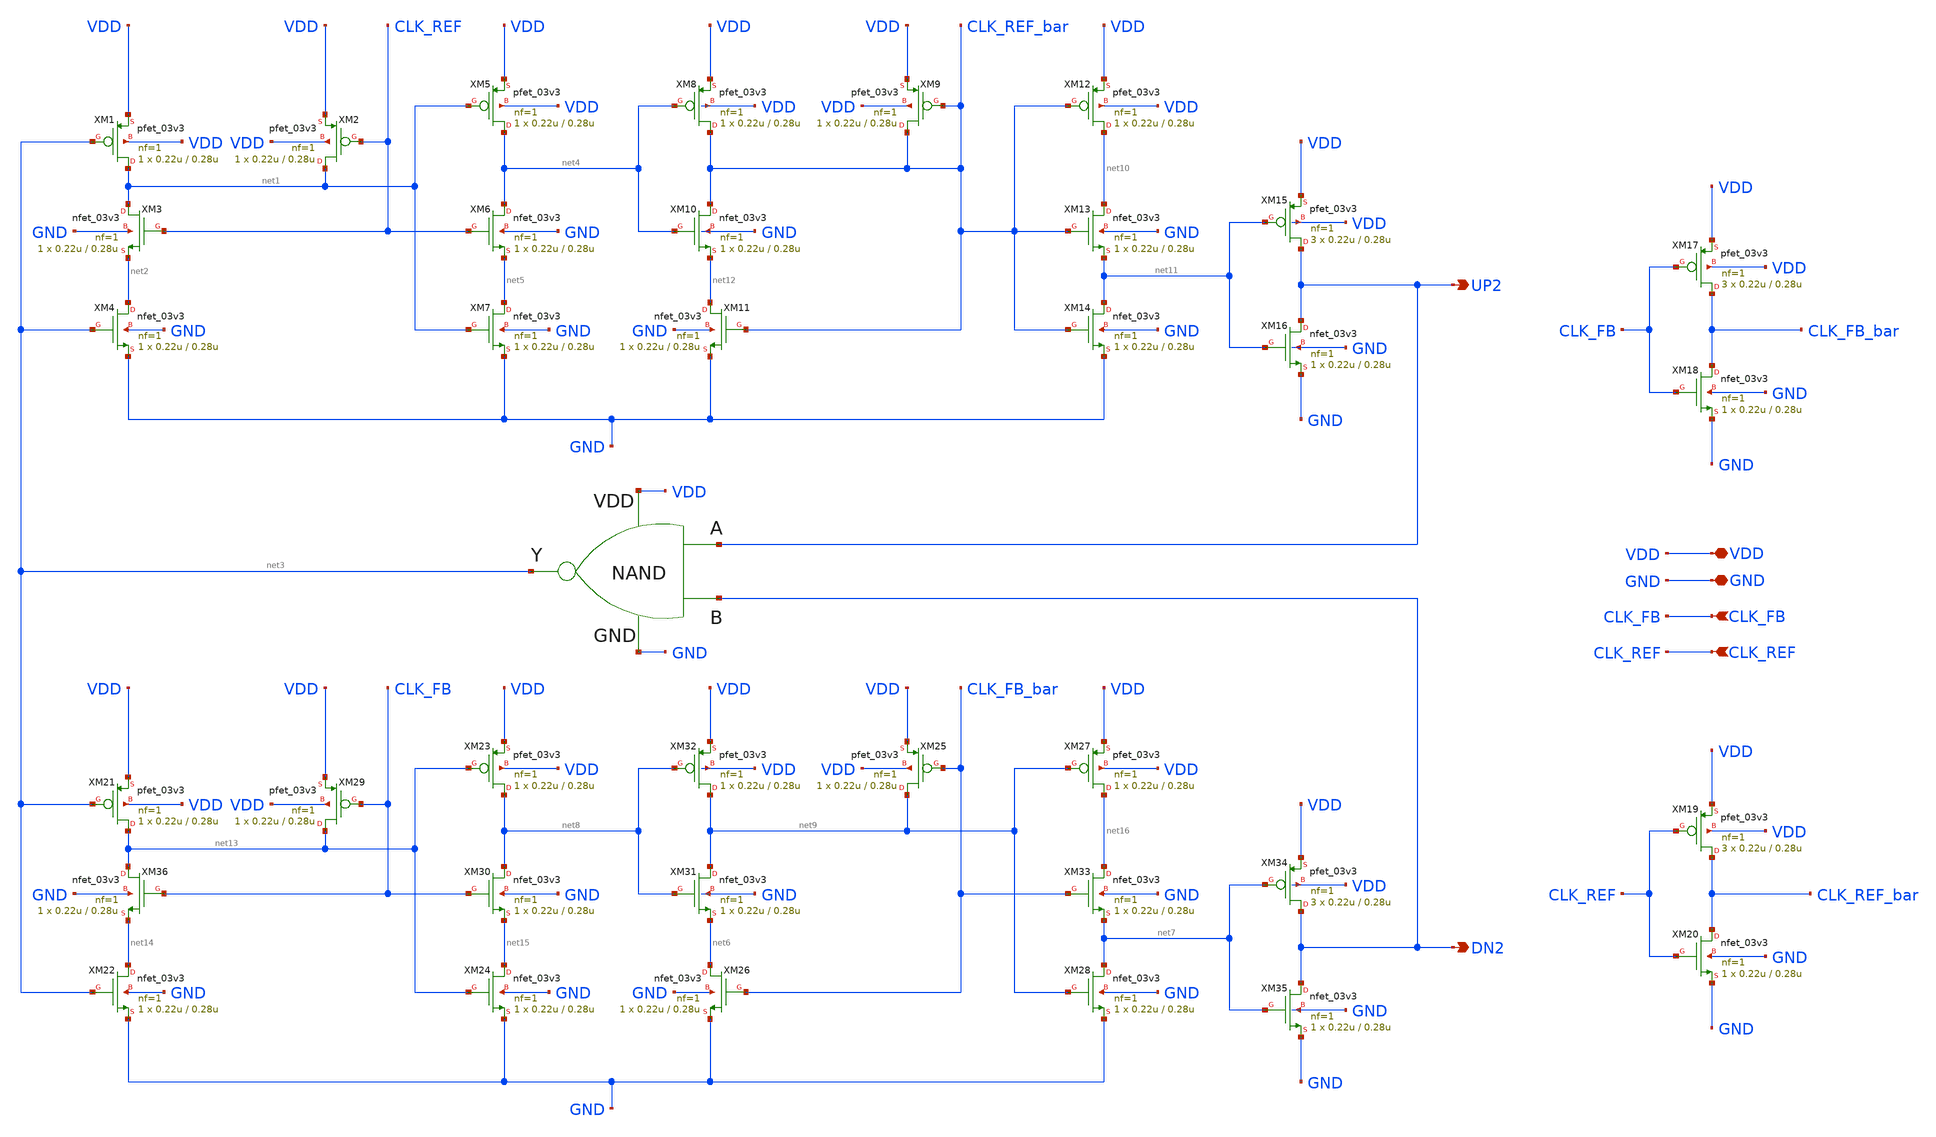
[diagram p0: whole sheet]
** sch_path: PFD/OPL_PFD.sch
**.subckt OPL_PFD UP2 CLK_FB CLK_REF DN2 VDD GND
*.opin UP2
*.ipin CLK_FB
*.ipin CLK_REF
*.opin DN2
*.iopin VDD
*.iopin GND
XM1 net1 net3 VDD VDD pfet_03v3 L=0.28u W=0.22u nf=1 ad='int((nf+1)/2) * W/nf * 0.18u' as='int((nf+2)/2) * W/nf * 0.18u'
+ pd='2*int((nf+1)/2) * (W/nf + 0.18u)' ps='2*int((nf+2)/2) * (W/nf + 0.18u)' nrd='0.18u / W' nrs='0.18u / W'
+ sa=0 sb=0 sd=0 m=1
XM4 net2 net3 GND GND nfet_03v3 L=0.28u W=0.22u nf=1 ad='int((nf+1)/2) * W/nf * 0.18u' as='int((nf+2)/2) * W/nf * 0.18u'
+ pd='2*int((nf+1)/2) * (W/nf + 0.18u)' ps='2*int((nf+2)/2) * (W/nf + 0.18u)' nrd='0.18u / W' nrs='0.18u / W'
+ sa=0 sb=0 sd=0 m=1
XM5 net4 net1 VDD VDD pfet_03v3 L=0.28u W=0.22u nf=1 ad='int((nf+1)/2) * W/nf * 0.18u' as='int((nf+2)/2) * W/nf * 0.18u'
+ pd='2*int((nf+1)/2) * (W/nf + 0.18u)' ps='2*int((nf+2)/2) * (W/nf + 0.18u)' nrd='0.18u / W' nrs='0.18u / W'
+ sa=0 sb=0 sd=0 m=1
XM7 net5 net1 GND GND nfet_03v3 L=0.28u W=0.22u nf=1 ad='int((nf+1)/2) * W/nf * 0.18u' as='int((nf+2)/2) * W/nf * 0.18u'
+ pd='2*int((nf+1)/2) * (W/nf + 0.18u)' ps='2*int((nf+2)/2) * (W/nf + 0.18u)' nrd='0.18u / W' nrs='0.18u / W'
+ sa=0 sb=0 sd=0 m=1
XM9 CLK_REF_bar CLK_REF_bar VDD VDD pfet_03v3 L=0.28u W=0.22u nf=1 ad='int((nf+1)/2) * W/nf * 0.18u'
+ as='int((nf+2)/2) * W/nf * 0.18u' pd='2*int((nf+1)/2) * (W/nf + 0.18u)' ps='2*int((nf+2)/2) * (W/nf + 0.18u)'
+ nrd='0.18u / W' nrs='0.18u / W' sa=0 sb=0 sd=0 m=1
XM11 net12 CLK_REF_bar GND GND nfet_03v3 L=0.28u W=0.22u nf=1 ad='int((nf+1)/2) * W/nf * 0.18u' as='int((nf+2)/2) * W/nf * 0.18u'
+ pd='2*int((nf+1)/2) * (W/nf + 0.18u)' ps='2*int((nf+2)/2) * (W/nf + 0.18u)' nrd='0.18u / W' nrs='0.18u / W'
+ sa=0 sb=0 sd=0 m=1
XM12 net10 CLK_REF_bar VDD VDD pfet_03v3 L=0.28u W=0.22u nf=1 ad='int((nf+1)/2) * W/nf * 0.18u' as='int((nf+2)/2) * W/nf * 0.18u'
+ pd='2*int((nf+1)/2) * (W/nf + 0.18u)' ps='2*int((nf+2)/2) * (W/nf + 0.18u)' nrd='0.18u / W' nrs='0.18u / W'
+ sa=0 sb=0 sd=0 m=1
XM14 net11 CLK_REF_bar GND GND nfet_03v3 L=0.28u W=0.22u nf=1 ad='int((nf+1)/2) * W/nf * 0.18u' as='int((nf+2)/2) * W/nf * 0.18u'
+ pd='2*int((nf+1)/2) * (W/nf + 0.18u)' ps='2*int((nf+2)/2) * (W/nf + 0.18u)' nrd='0.18u / W' nrs='0.18u / W'
+ sa=0 sb=0 sd=0 m=1
XM2 net1 CLK_REF VDD VDD pfet_03v3 L=0.28u W=0.22u nf=1 ad='int((nf+1)/2) * W/nf * 0.18u' as='int((nf+2)/2) * W/nf * 0.18u'
+ pd='2*int((nf+1)/2) * (W/nf + 0.18u)' ps='2*int((nf+2)/2) * (W/nf + 0.18u)' nrd='0.18u / W' nrs='0.18u / W'
+ sa=0 sb=0 sd=0 m=1
XM6 net4 CLK_REF net5 GND nfet_03v3 L=0.28u W=0.22u nf=1 ad='int((nf+1)/2) * W/nf * 0.18u' as='int((nf+2)/2) * W/nf * 0.18u'
+ pd='2*int((nf+1)/2) * (W/nf + 0.18u)' ps='2*int((nf+2)/2) * (W/nf + 0.18u)' nrd='0.18u / W' nrs='0.18u / W'
+ sa=0 sb=0 sd=0 m=1
XM10 CLK_REF_bar net4 net12 GND nfet_03v3 L=0.28u W=0.22u nf=1 ad='int((nf+1)/2) * W/nf * 0.18u' as='int((nf+2)/2) * W/nf * 0.18u'
+ pd='2*int((nf+1)/2) * (W/nf + 0.18u)' ps='2*int((nf+2)/2) * (W/nf + 0.18u)' nrd='0.18u / W' nrs='0.18u / W'
+ sa=0 sb=0 sd=0 m=1
XM8 CLK_REF_bar net4 VDD VDD pfet_03v3 L=0.28u W=0.22u nf=1 ad='int((nf+1)/2) * W/nf * 0.18u' as='int((nf+2)/2) * W/nf * 0.18u'
+ pd='2*int((nf+1)/2) * (W/nf + 0.18u)' ps='2*int((nf+2)/2) * (W/nf + 0.18u)' nrd='0.18u / W' nrs='0.18u / W'
+ sa=0 sb=0 sd=0 m=1
XM13 net10 CLK_REF_bar net11 GND nfet_03v3 L=0.28u W=0.22u nf=1 ad='int((nf+1)/2) * W/nf * 0.18u' as='int((nf+2)/2) * W/nf * 0.18u'
+ pd='2*int((nf+1)/2) * (W/nf + 0.18u)' ps='2*int((nf+2)/2) * (W/nf + 0.18u)' nrd='0.18u / W' nrs='0.18u / W'
+ sa=0 sb=0 sd=0 m=1
XM15 UP2 net11 VDD VDD pfet_03v3 L=0.28u W=0.22u nf=1 ad='int((nf+1)/2) * W/nf * 0.18u' as='int((nf+2)/2) * W/nf * 0.18u'
+ pd='2*int((nf+1)/2) * (W/nf + 0.18u)' ps='2*int((nf+2)/2) * (W/nf + 0.18u)' nrd='0.18u / W' nrs='0.18u / W'
+ sa=0 sb=0 sd=0 m=3
XM16 UP2 net11 GND GND nfet_03v3 L=0.28u W=0.22u nf=1 ad='int((nf+1)/2) * W/nf * 0.18u' as='int((nf+2)/2) * W/nf * 0.18u'
+ pd='2*int((nf+1)/2) * (W/nf + 0.18u)' ps='2*int((nf+2)/2) * (W/nf + 0.18u)' nrd='0.18u / W' nrs='0.18u / W'
+ sa=0 sb=0 sd=0 m=1
XM17 CLK_FB_bar CLK_FB VDD VDD pfet_03v3 L=0.28u W=0.22u nf=1 ad='int((nf+1)/2) * W/nf * 0.18u' as='int((nf+2)/2) * W/nf * 0.18u'
+ pd='2*int((nf+1)/2) * (W/nf + 0.18u)' ps='2*int((nf+2)/2) * (W/nf + 0.18u)' nrd='0.18u / W' nrs='0.18u / W'
+ sa=0 sb=0 sd=0 m=3
XM18 CLK_FB_bar CLK_FB GND GND nfet_03v3 L=0.28u W=0.22u nf=1 ad='int((nf+1)/2) * W/nf * 0.18u' as='int((nf+2)/2) * W/nf * 0.18u'
+ pd='2*int((nf+1)/2) * (W/nf + 0.18u)' ps='2*int((nf+2)/2) * (W/nf + 0.18u)' nrd='0.18u / W' nrs='0.18u / W'
+ sa=0 sb=0 sd=0 m=1
XM19 CLK_REF_bar CLK_REF VDD VDD pfet_03v3 L=0.28u W=0.22u nf=1 ad='int((nf+1)/2) * W/nf * 0.18u' as='int((nf+2)/2) * W/nf * 0.18u'
+ pd='2*int((nf+1)/2) * (W/nf + 0.18u)' ps='2*int((nf+2)/2) * (W/nf + 0.18u)' nrd='0.18u / W' nrs='0.18u / W'
+ sa=0 sb=0 sd=0 m=3
XM20 CLK_REF_bar CLK_REF GND GND nfet_03v3 L=0.28u W=0.22u nf=1 ad='int((nf+1)/2) * W/nf * 0.18u' as='int((nf+2)/2) * W/nf * 0.18u'
+ pd='2*int((nf+1)/2) * (W/nf + 0.18u)' ps='2*int((nf+2)/2) * (W/nf + 0.18u)' nrd='0.18u / W' nrs='0.18u / W'
+ sa=0 sb=0 sd=0 m=1
XM3 net1 CLK_REF net2 GND nfet_03v3 L=0.28u W=0.22u nf=1 ad='int((nf+1)/2) * W/nf * 0.18u' as='int((nf+2)/2) * W/nf * 0.18u'
+ pd='2*int((nf+1)/2) * (W/nf + 0.18u)' ps='2*int((nf+2)/2) * (W/nf + 0.18u)' nrd='0.18u / W' nrs='0.18u / W'
+ sa=0 sb=0 sd=0 m=1
XM21 net13 net3 VDD VDD pfet_03v3 L=0.28u W=0.22u nf=1 ad='int((nf+1)/2) * W/nf * 0.18u' as='int((nf+2)/2) * W/nf * 0.18u'
+ pd='2*int((nf+1)/2) * (W/nf + 0.18u)' ps='2*int((nf+2)/2) * (W/nf + 0.18u)' nrd='0.18u / W' nrs='0.18u / W'
+ sa=0 sb=0 sd=0 m=1
XM22 net14 net3 GND GND nfet_03v3 L=0.28u W=0.22u nf=1 ad='int((nf+1)/2) * W/nf * 0.18u' as='int((nf+2)/2) * W/nf * 0.18u'
+ pd='2*int((nf+1)/2) * (W/nf + 0.18u)' ps='2*int((nf+2)/2) * (W/nf + 0.18u)' nrd='0.18u / W' nrs='0.18u / W'
+ sa=0 sb=0 sd=0 m=1
XM23 net8 net13 VDD VDD pfet_03v3 L=0.28u W=0.22u nf=1 ad='int((nf+1)/2) * W/nf * 0.18u' as='int((nf+2)/2) * W/nf * 0.18u'
+ pd='2*int((nf+1)/2) * (W/nf + 0.18u)' ps='2*int((nf+2)/2) * (W/nf + 0.18u)' nrd='0.18u / W' nrs='0.18u / W'
+ sa=0 sb=0 sd=0 m=1
XM24 net15 net13 GND GND nfet_03v3 L=0.28u W=0.22u nf=1 ad='int((nf+1)/2) * W/nf * 0.18u' as='int((nf+2)/2) * W/nf * 0.18u'
+ pd='2*int((nf+1)/2) * (W/nf + 0.18u)' ps='2*int((nf+2)/2) * (W/nf + 0.18u)' nrd='0.18u / W' nrs='0.18u / W'
+ sa=0 sb=0 sd=0 m=1
XM25 net9 CLK_FB_bar VDD VDD pfet_03v3 L=0.28u W=0.22u nf=1 ad='int((nf+1)/2) * W/nf * 0.18u' as='int((nf+2)/2) * W/nf * 0.18u'
+ pd='2*int((nf+1)/2) * (W/nf + 0.18u)' ps='2*int((nf+2)/2) * (W/nf + 0.18u)' nrd='0.18u / W' nrs='0.18u / W'
+ sa=0 sb=0 sd=0 m=1
XM26 net6 CLK_FB_bar GND GND nfet_03v3 L=0.28u W=0.22u nf=1 ad='int((nf+1)/2) * W/nf * 0.18u' as='int((nf+2)/2) * W/nf * 0.18u'
+ pd='2*int((nf+1)/2) * (W/nf + 0.18u)' ps='2*int((nf+2)/2) * (W/nf + 0.18u)' nrd='0.18u / W' nrs='0.18u / W'
+ sa=0 sb=0 sd=0 m=1
XM27 net16 net9 VDD VDD pfet_03v3 L=0.28u W=0.22u nf=1 ad='int((nf+1)/2) * W/nf * 0.18u' as='int((nf+2)/2) * W/nf * 0.18u'
+ pd='2*int((nf+1)/2) * (W/nf + 0.18u)' ps='2*int((nf+2)/2) * (W/nf + 0.18u)' nrd='0.18u / W' nrs='0.18u / W'
+ sa=0 sb=0 sd=0 m=1
XM28 net7 net9 GND GND nfet_03v3 L=0.28u W=0.22u nf=1 ad='int((nf+1)/2) * W/nf * 0.18u' as='int((nf+2)/2) * W/nf * 0.18u'
+ pd='2*int((nf+1)/2) * (W/nf + 0.18u)' ps='2*int((nf+2)/2) * (W/nf + 0.18u)' nrd='0.18u / W' nrs='0.18u / W'
+ sa=0 sb=0 sd=0 m=1
XM29 net13 CLK_FB VDD VDD pfet_03v3 L=0.28u W=0.22u nf=1 ad='int((nf+1)/2) * W/nf * 0.18u' as='int((nf+2)/2) * W/nf * 0.18u'
+ pd='2*int((nf+1)/2) * (W/nf + 0.18u)' ps='2*int((nf+2)/2) * (W/nf + 0.18u)' nrd='0.18u / W' nrs='0.18u / W'
+ sa=0 sb=0 sd=0 m=1
XM30 net8 CLK_FB net15 GND nfet_03v3 L=0.28u W=0.22u nf=1 ad='int((nf+1)/2) * W/nf * 0.18u' as='int((nf+2)/2) * W/nf * 0.18u'
+ pd='2*int((nf+1)/2) * (W/nf + 0.18u)' ps='2*int((nf+2)/2) * (W/nf + 0.18u)' nrd='0.18u / W' nrs='0.18u / W'
+ sa=0 sb=0 sd=0 m=1
XM31 net9 net8 net6 GND nfet_03v3 L=0.28u W=0.22u nf=1 ad='int((nf+1)/2) * W/nf * 0.18u' as='int((nf+2)/2) * W/nf * 0.18u'
+ pd='2*int((nf+1)/2) * (W/nf + 0.18u)' ps='2*int((nf+2)/2) * (W/nf + 0.18u)' nrd='0.18u / W' nrs='0.18u / W'
+ sa=0 sb=0 sd=0 m=1
XM32 net9 net8 VDD VDD pfet_03v3 L=0.28u W=0.22u nf=1 ad='int((nf+1)/2) * W/nf * 0.18u' as='int((nf+2)/2) * W/nf * 0.18u'
+ pd='2*int((nf+1)/2) * (W/nf + 0.18u)' ps='2*int((nf+2)/2) * (W/nf + 0.18u)' nrd='0.18u / W' nrs='0.18u / W'
+ sa=0 sb=0 sd=0 m=1
XM33 net16 CLK_FB_bar net7 GND nfet_03v3 L=0.28u W=0.22u nf=1 ad='int((nf+1)/2) * W/nf * 0.18u' as='int((nf+2)/2) * W/nf * 0.18u'
+ pd='2*int((nf+1)/2) * (W/nf + 0.18u)' ps='2*int((nf+2)/2) * (W/nf + 0.18u)' nrd='0.18u / W' nrs='0.18u / W'
+ sa=0 sb=0 sd=0 m=1
XM34 DN2 net7 VDD VDD pfet_03v3 L=0.28u W=0.22u nf=1 ad='int((nf+1)/2) * W/nf * 0.18u' as='int((nf+2)/2) * W/nf * 0.18u'
+ pd='2*int((nf+1)/2) * (W/nf + 0.18u)' ps='2*int((nf+2)/2) * (W/nf + 0.18u)' nrd='0.18u / W' nrs='0.18u / W'
+ sa=0 sb=0 sd=0 m=3
XM35 DN2 net7 GND GND nfet_03v3 L=0.28u W=0.22u nf=1 ad='int((nf+1)/2) * W/nf * 0.18u' as='int((nf+2)/2) * W/nf * 0.18u'
+ pd='2*int((nf+1)/2) * (W/nf + 0.18u)' ps='2*int((nf+2)/2) * (W/nf + 0.18u)' nrd='0.18u / W' nrs='0.18u / W'
+ sa=0 sb=0 sd=0 m=1
XM36 net13 CLK_FB net14 GND nfet_03v3 L=0.28u W=0.22u nf=1 ad='int((nf+1)/2) * W/nf * 0.18u' as='int((nf+2)/2) * W/nf * 0.18u'
+ pd='2*int((nf+1)/2) * (W/nf + 0.18u)' ps='2*int((nf+2)/2) * (W/nf + 0.18u)' nrd='0.18u / W' nrs='0.18u / W'
+ sa=0 sb=0 sd=0 m=1
x1 GND UP2 DN2 VDD net3 NAND
**.ends

* expanding   symbol:  NAND.sym # of pins=5
** sym_path: PFD/NAND.sym
** sch_path: PFD/NAND.sch
.subckt NAND GND A B VDD Y
*.opin Y
*.ipin A
*.ipin B
*.iopin VDD
*.iopin GND
XM1 Y A net2 VDD pfet_03v3 L=0.28u W=0.22u nf=1 ad='int((nf+1)/2) * W/nf * 0.18u' as='int((nf+2)/2) * W/nf * 0.18u'
+ pd='2*int((nf+1)/2) * (W/nf + 0.18u)' ps='2*int((nf+2)/2) * (W/nf + 0.18u)' nrd='0.18u / W' nrs='0.18u / W'
+ sa=0 sb=0 sd=0 m=3
XM3 Y A net1 GND nfet_03v3 L=0.28u W=0.22u nf=1 ad='int((nf+1)/2) * W/nf * 0.18u' as='int((nf+2)/2) * W/nf * 0.18u'
+ pd='2*int((nf+1)/2) * (W/nf + 0.18u)' ps='2*int((nf+2)/2) * (W/nf + 0.18u)' nrd='0.18u / W' nrs='0.18u / W'
+ sa=0 sb=0 sd=0 m=1
XM4 net1 B GND GND nfet_03v3 L=0.28u W=0.22u nf=1 ad='int((nf+1)/2) * W/nf * 0.18u' as='int((nf+2)/2) * W/nf * 0.18u'
+ pd='2*int((nf+1)/2) * (W/nf + 0.18u)' ps='2*int((nf+2)/2) * (W/nf + 0.18u)' nrd='0.18u / W' nrs='0.18u / W'
+ sa=0 sb=0 sd=0 m=1
XM2 Y B net3 VDD pfet_03v3 L=0.28u W=0.22u nf=1 ad='int((nf+1)/2) * W/nf * 0.18u' as='int((nf+2)/2) * W/nf * 0.18u'
+ pd='2*int((nf+1)/2) * (W/nf + 0.18u)' ps='2*int((nf+2)/2) * (W/nf + 0.18u)' nrd='0.18u / W' nrs='0.18u / W'
+ sa=0 sb=0 sd=0 m=3
.ends

.end
